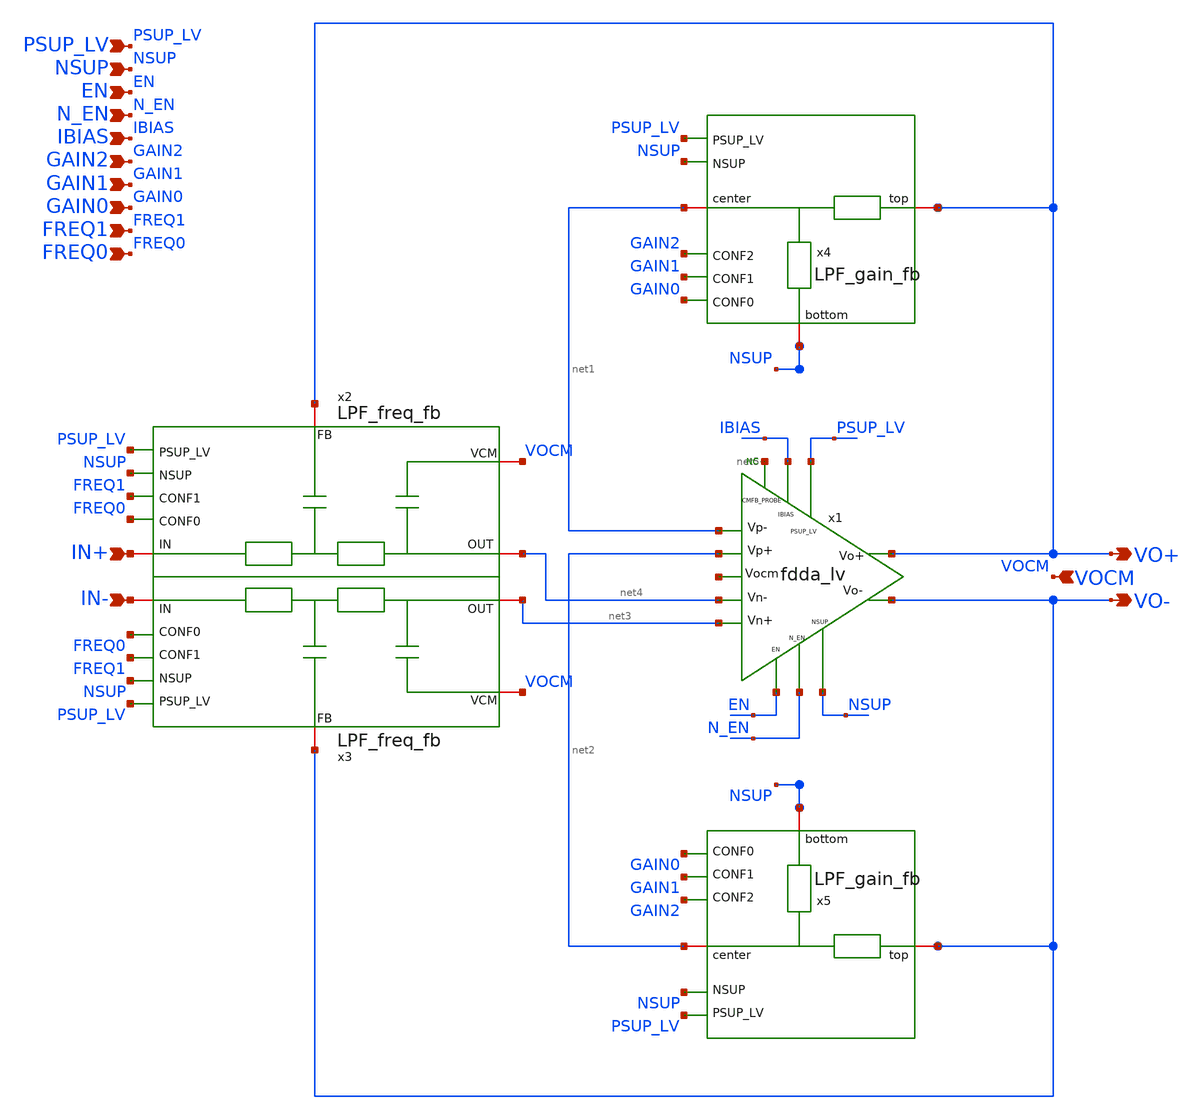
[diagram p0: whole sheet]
** sch_path: xschem/blocks/LPF/LPF.sch
**.subckt LPF NSUP EN N_EN IBIAS PSUP_LV GAIN2 VO+ VO- VOCM GAIN1 GAIN0 FREQ1 FREQ0 IN+ IN-
*.ipin NSUP
*.ipin EN
*.ipin N_EN
*.ipin IBIAS
*.ipin PSUP_LV
*.ipin GAIN2
*.opin VO+
*.opin VO-
*.ipin VOCM
*.ipin GAIN1
*.ipin GAIN0
*.ipin FREQ1
*.ipin FREQ0
*.ipin IN+
*.ipin IN-
* noconn #net5
x1 PSUP_LV net1 net4 net3 net2 VO+ VO- IBIAS N_EN EN NSUP net5 net6 fdda_lv
x2 VO+ PSUP_LV NSUP net4 IN+ FREQ1 FREQ0 VOCM LPF_freq_fb
x3 VO- PSUP_LV NSUP net3 IN- FREQ1 FREQ0 VOCM LPF_freq_fb
x4 VO+ net1 PSUP_LV NSUP GAIN2 GAIN1 GAIN0 NSUP LPF_gain_fb
x5 VO- net2 PSUP_LV NSUP GAIN2 GAIN1 GAIN0 NSUP LPF_gain_fb
**.ends
.end
